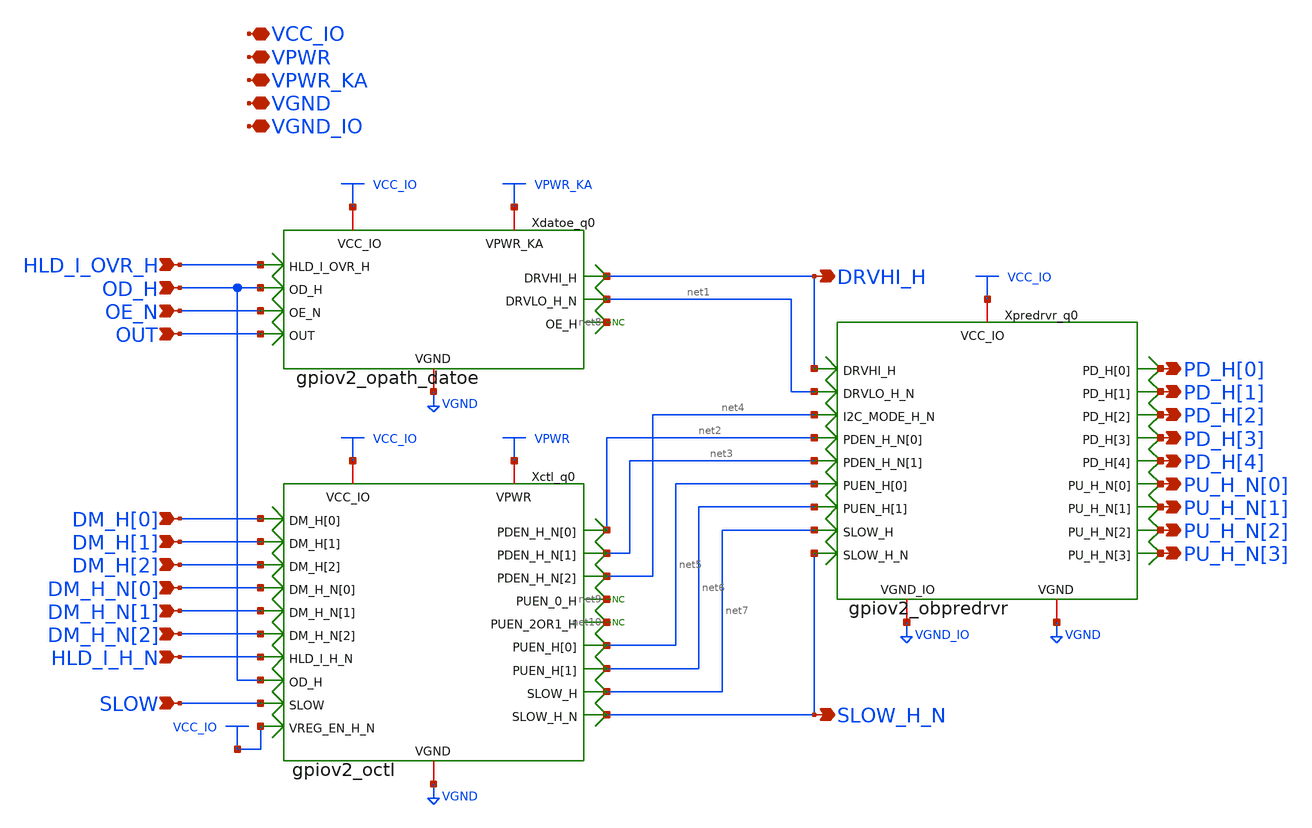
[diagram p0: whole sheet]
** sch_path: gpiov2_octl_dat.sch
* Copyright 2023 David Mitchell Bailey
* Licensed under the Apache License, Version 2.0 (the "License");
* you may not use this file except in compliance with the License.
* You may obtain a copy of the License at
* https://www.apache.org/licenses/LICENSE-2.0
* Unless required by applicable law or agreed to in writing, software
* distributed under the License is distributed on an "AS IS" BASIS,
* WITHOUT WARRANTIES OR CONDITIONS OF ANY KIND, either express or implied.
* See the License for the specific language governing permissions and
* limitations under the License.
**.subckt gpiov2_octl_dat VPWR HLD_I_OVR_H DRVHI_H OD_H OE_N OUT DM_H[0] DM_H[1] DM_H[2] DM_H_N[0]
*+ DM_H_N[1] DM_H_N[2] HLD_I_H_N SLOW PD_H[0] PD_H[1] PD_H[2] PD_H[3] PD_H[4] PU_H_N[0] PU_H_N[1] PU_H_N[2]
*+ PU_H_N[3] SLOW_H_N VPWR_KA VGND VGND_IO VCC_IO
*.iopin VPWR
*.ipin HLD_I_OVR_H
*.opin DRVHI_H
*.ipin OD_H
*.ipin OE_N
*.ipin OUT
*.ipin DM_H[0]
*.ipin DM_H[1]
*.ipin DM_H[2]
*.ipin DM_H_N[0]
*.ipin DM_H_N[1]
*.ipin DM_H_N[2]
*.ipin HLD_I_H_N
*.ipin SLOW
*.opin PD_H[0]
*.opin PD_H[1]
*.opin PD_H[2]
*.opin PD_H[3]
*.opin PD_H[4]
*.opin PU_H_N[0]
*.opin PU_H_N[1]
*.opin PU_H_N[2]
*.opin PU_H_N[3]
*.opin SLOW_H_N
*.iopin VPWR_KA
*.iopin VGND
*.iopin VGND_IO
*.iopin VCC_IO
Xdatoe_q0 VCC_IO VPWR_KA VGND HLD_I_OVR_H OE_N net8 OD_H DRVHI_H net1 OUT gpiov2_opath_datoe
Xctl_q0 VCC_IO VPWR VGND net2 DM_H[0] DM_H[1] DM_H[2] DM_H_N[0] net3 DM_H_N[1] DM_H_N[2] net4
+ HLD_I_H_N SLOW net7 OD_H SLOW_H_N net5 net9 net10 net6 VCC_IO gpiov2_octl
Xpredrvr_q0 VCC_IO VGND_IO VGND net1 DRVHI_H PD_H[2] net4 PU_H_N[2] net6 PD_H[3] net3 PU_H_N[3]
+ PD_H[4] SLOW_H_N net7 PU_H_N[1] PD_H[1] net2 net5 PU_H_N[0] PD_H[0] gpiov2_obpredrvr
* noconn #net8
* noconn #net9
* noconn #net10
**.ends
.end
